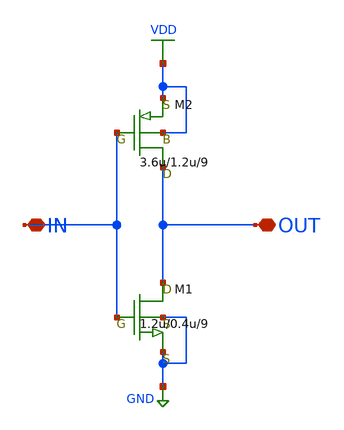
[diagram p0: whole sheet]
** sch_path: LR_hasegawa/LR_Work2/Citizen035/INVERTER9_Citizen.sch
**.subckt INVERTER9_Citizen OUT IN
*.iopin OUT
*.iopin IN
M1 OUT IN GND GND nch w=1.2u l=0.4u as=0 ps=0 ad=0 pd=0 m=9
M2 OUT IN VDD VDD pch w=3.6u l=1.2u as=0 ps=0 ad=0 pd=0 m=9
**.ends
.GLOBAL VDD
.GLOBAL GND
.end
